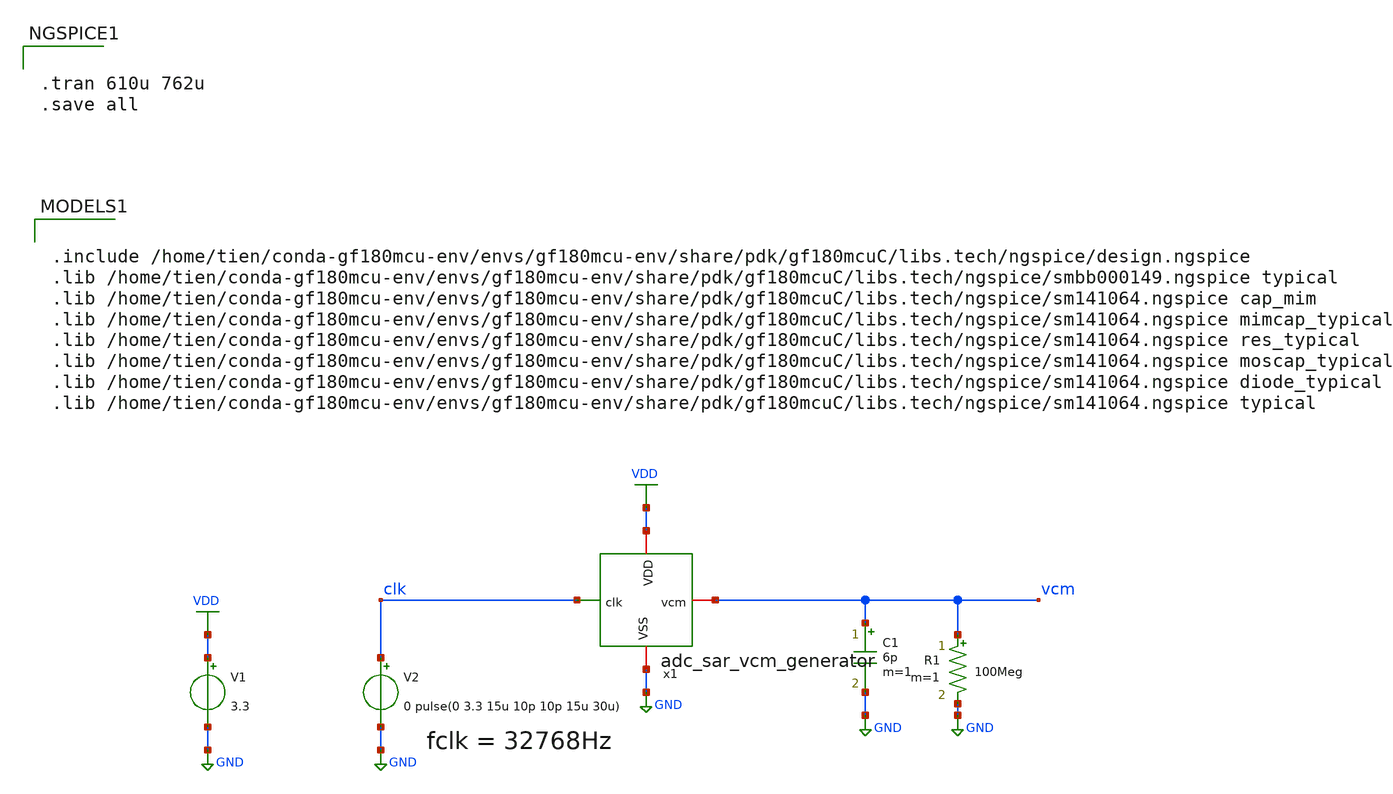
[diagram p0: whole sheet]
** sch_path: adc_sar_vcm_generator_tb.sch
**.subckt adc_sar_vcm_generator_tb
V1 VDD GND 3.3
V2 clk GND 0 pulse(0 3.3 15u 10p 10p 15u 30u)
C1 vcm GND 6p m=1
R1 vcm GND 100Meg m=1
x1 VDD vcm clk GND adc_sar_vcm_generator
**** begin user architecture code


.tran 610u 762u
.save all



.include /home/tien/conda-gf180mcu-env/envs/gf180mcu-env/share/pdk/gf180mcuC/libs.tech/ngspice/design.ngspice
.lib /home/tien/conda-gf180mcu-env/envs/gf180mcu-env/share/pdk/gf180mcuC/libs.tech/ngspice/smbb000149.ngspice typical
.lib /home/tien/conda-gf180mcu-env/envs/gf180mcu-env/share/pdk/gf180mcuC/libs.tech/ngspice/sm141064.ngspice cap_mim
.lib /home/tien/conda-gf180mcu-env/envs/gf180mcu-env/share/pdk/gf180mcuC/libs.tech/ngspice/sm141064.ngspice mimcap_typical
.lib /home/tien/conda-gf180mcu-env/envs/gf180mcu-env/share/pdk/gf180mcuC/libs.tech/ngspice/sm141064.ngspice res_typical
.lib /home/tien/conda-gf180mcu-env/envs/gf180mcu-env/share/pdk/gf180mcuC/libs.tech/ngspice/sm141064.ngspice moscap_typical
.lib /home/tien/conda-gf180mcu-env/envs/gf180mcu-env/share/pdk/gf180mcuC/libs.tech/ngspice/sm141064.ngspice diode_typical
.lib /home/tien/conda-gf180mcu-env/envs/gf180mcu-env/share/pdk/gf180mcuC/libs.tech/ngspice/sm141064.ngspice typical

**** end user architecture code
**.ends
.GLOBAL GND
.GLOBAL VDD
.end
